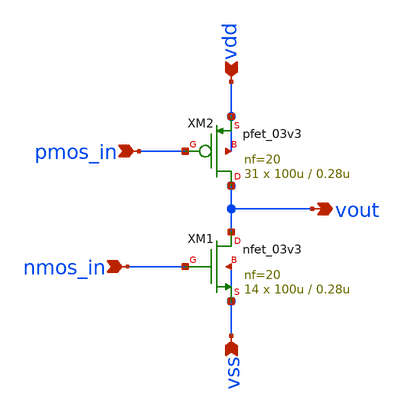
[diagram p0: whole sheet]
** sch_path: designs/libs/core_analog/Output_Stage/Output_Stage_2.sch
**.subckt Output_Stage_2 nmos_in pmos_in vdd vss vout
*.ipin nmos_in
*.ipin pmos_in
*.ipin vdd
*.ipin vss
*.opin vout
XM1 vout nmos_in vss vss nfet_03v3 L=0.28u W=100u nf=20 ad='int((nf+1)/2) * W/nf * 0.18u' as='int((nf+2)/2) * W/nf * 0.18u'
+ pd='2*int((nf+1)/2) * (W/nf + 0.18u)' ps='2*int((nf+2)/2) * (W/nf + 0.18u)' nrd='0.18u / W' nrs='0.18u / W'
+ sa=0 sb=0 sd=0 m=14
XM2 vout pmos_in vdd vdd pfet_03v3 L=0.28u W=100u nf=20 ad='int((nf+1)/2) * W/nf * 0.18u' as='int((nf+2)/2) * W/nf * 0.18u'
+ pd='2*int((nf+1)/2) * (W/nf + 0.18u)' ps='2*int((nf+2)/2) * (W/nf + 0.18u)' nrd='0.18u / W' nrs='0.18u / W'
+ sa=0 sb=0 sd=0 m=31
**.ends
.end
